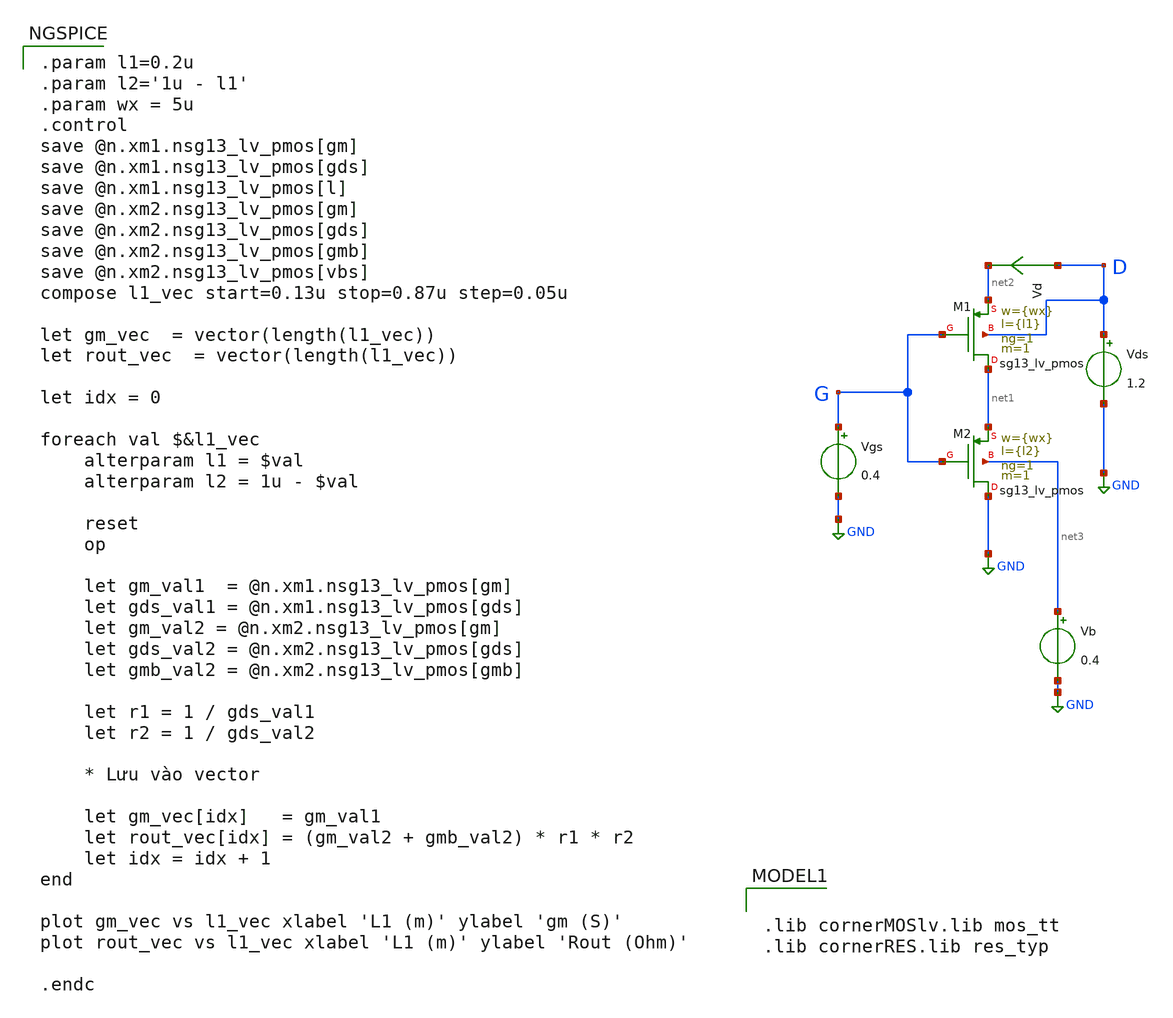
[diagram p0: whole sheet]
** sch_path: xschem/self-cascode-pmos.sch
**.subckt self-cascode-pmos
Vgs G GND 0.4
Vds D GND 1.2
Vd D net2 0
.save i(vd)
Vb net3 GND 0.4
XM1 net1 G net2 D sg13_lv_pmos w={wx} l={l1} ng=1 m=1 mm_ok=1
XM2 GND G net1 net3 sg13_lv_pmos w={wx} l={l2} ng=1 m=1 mm_ok=1
**** begin user architecture code

.lib cornerMOSlv.lib mos_tt
.lib cornerRES.lib res_typ


.param l1=0.2u
.param l2='1u - l1'
.param wx = 5u
.control
save @n.xm1.nsg13_lv_pmos[gm]
save @n.xm1.nsg13_lv_pmos[gds]
save @n.xm1.nsg13_lv_pmos[l]
save @n.xm2.nsg13_lv_pmos[gm]
save @n.xm2.nsg13_lv_pmos[gds]
save @n.xm2.nsg13_lv_pmos[gmb]
save @n.xm2.nsg13_lv_pmos[vbs]
compose l1_vec start=0.13u stop=0.87u step=0.05u

let gm_vec  = vector(length(l1_vec))
let rout_vec  = vector(length(l1_vec))

let idx = 0

foreach val $&l1_vec
    alterparam l1 = $val
    alterparam l2 = 1u - $val

    reset
    op

    let gm_val1  = @n.xm1.nsg13_lv_pmos[gm]
    let gds_val1 = @n.xm1.nsg13_lv_pmos[gds]
    let gm_val2 = @n.xm2.nsg13_lv_pmos[gm]
    let gds_val2 = @n.xm2.nsg13_lv_pmos[gds]
    let gmb_val2 = @n.xm2.nsg13_lv_pmos[gmb]

    let r1 = 1 / gds_val1
    let r2 = 1 / gds_val2

    * Lưu vào vector

    let gm_vec[idx]   = gm_val1
    let rout_vec[idx] = (gm_val2 + gmb_val2) * r1 * r2
    let idx = idx + 1
end

plot gm_vec vs l1_vec xlabel 'L1 (m)' ylabel 'gm (S)'
plot rout_vec vs l1_vec xlabel 'L1 (m)' ylabel 'Rout (Ohm)'

.endc


**** end user architecture code
**.ends
.GLOBAL GND
.end
